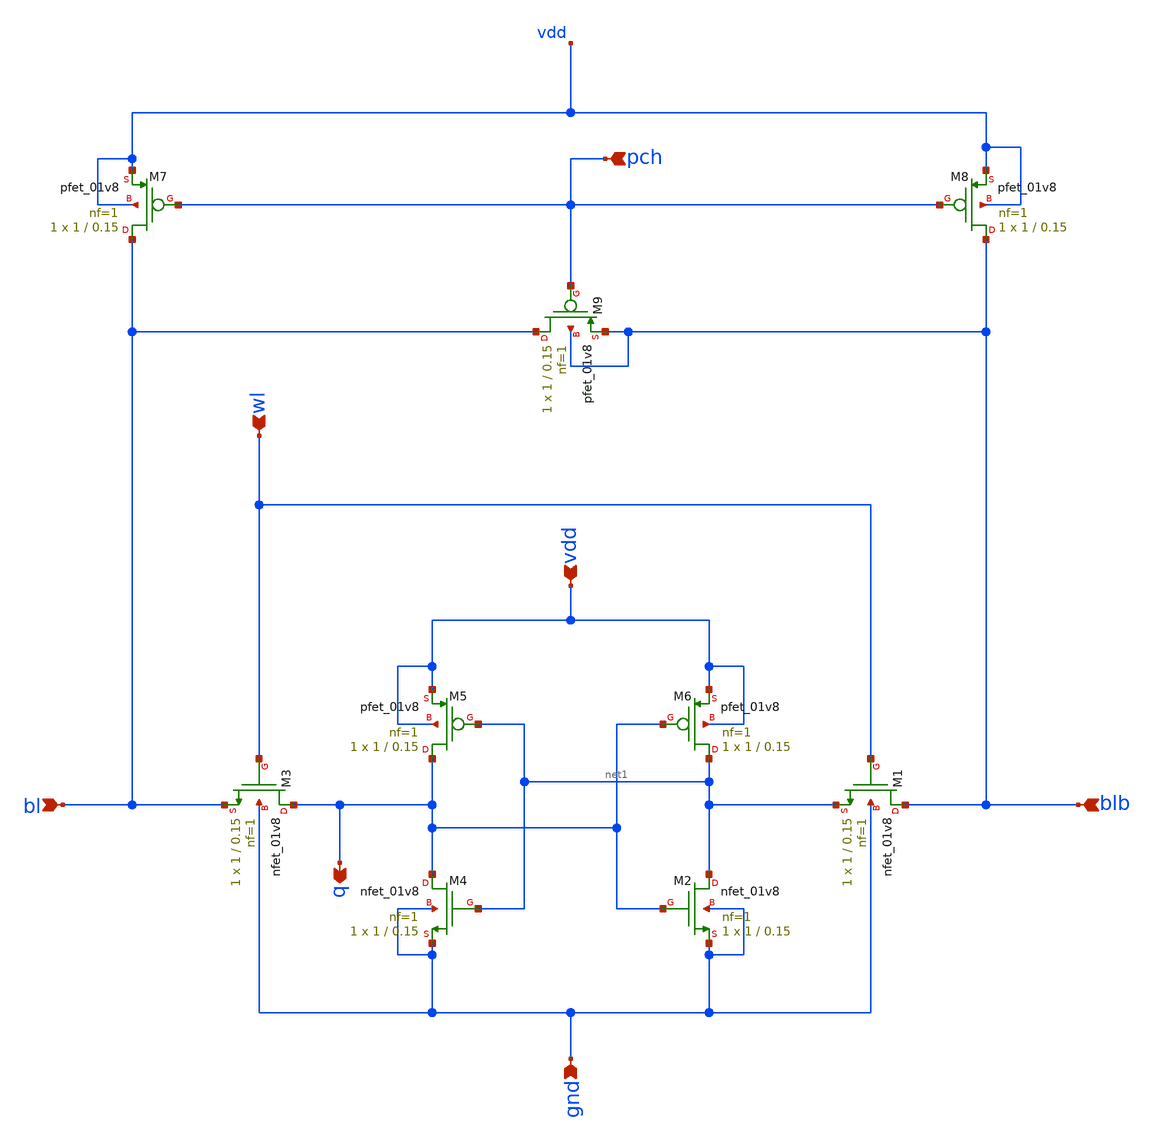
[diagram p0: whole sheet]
** sch_path: sram/sram_pch_1b.sch
**.subckt sram_pch_1b gnd bl blb vdd wl pch q
*.ipin gnd
*.ipin bl
*.ipin blb
*.ipin vdd
*.ipin wl
*.ipin pch
*.opin q
XM1 blb wl net1 gnd sky130_fd_pr__nfet_01v8 L=0.15 W=1 nf=1 ad='int((nf+1)/2) * W/nf * 0.29' as='int((nf+2)/2) * W/nf * 0.29'
+ pd='2*int((nf+1)/2) * (W/nf + 0.29)' ps='2*int((nf+2)/2) * (W/nf + 0.29)' nrd='0.29 / W' nrs='0.29 / W'
+ sa=0 sb=0 sd=0 mult=1 m=1
XM3 q wl bl gnd sky130_fd_pr__nfet_01v8 L=0.15 W=1 nf=1 ad='int((nf+1)/2) * W/nf * 0.29' as='int((nf+2)/2) * W/nf * 0.29'
+ pd='2*int((nf+1)/2) * (W/nf + 0.29)' ps='2*int((nf+2)/2) * (W/nf + 0.29)' nrd='0.29 / W' nrs='0.29 / W'
+ sa=0 sb=0 sd=0 mult=1 m=1
XM5 q net1 vdd vdd sky130_fd_pr__pfet_01v8 L=0.15 W=1 nf=1 ad='int((nf+1)/2) * W/nf * 0.29' as='int((nf+2)/2) * W/nf * 0.29'
+ pd='2*int((nf+1)/2) * (W/nf + 0.29)' ps='2*int((nf+2)/2) * (W/nf + 0.29)' nrd='0.29 / W' nrs='0.29 / W'
+ sa=0 sb=0 sd=0 mult=1 m=1
XM6 net1 q vdd vdd sky130_fd_pr__pfet_01v8 L=0.15 W=1 nf=1 ad='int((nf+1)/2) * W/nf * 0.29' as='int((nf+2)/2) * W/nf * 0.29'
+ pd='2*int((nf+1)/2) * (W/nf + 0.29)' ps='2*int((nf+2)/2) * (W/nf + 0.29)' nrd='0.29 / W' nrs='0.29 / W'
+ sa=0 sb=0 sd=0 mult=1 m=1
XM7 bl pch vdd vdd sky130_fd_pr__pfet_01v8 L=0.15 W=1 nf=1 ad='int((nf+1)/2) * W/nf * 0.29' as='int((nf+2)/2) * W/nf * 0.29'
+ pd='2*int((nf+1)/2) * (W/nf + 0.29)' ps='2*int((nf+2)/2) * (W/nf + 0.29)' nrd='0.29 / W' nrs='0.29 / W'
+ sa=0 sb=0 sd=0 mult=1 m=1
XM8 blb pch vdd vdd sky130_fd_pr__pfet_01v8 L=0.15 W=1 nf=1 ad='int((nf+1)/2) * W/nf * 0.29' as='int((nf+2)/2) * W/nf * 0.29'
+ pd='2*int((nf+1)/2) * (W/nf + 0.29)' ps='2*int((nf+2)/2) * (W/nf + 0.29)' nrd='0.29 / W' nrs='0.29 / W'
+ sa=0 sb=0 sd=0 mult=1 m=1
XM9 bl pch blb blb sky130_fd_pr__pfet_01v8 L=0.15 W=1 nf=1 ad='int((nf+1)/2) * W/nf * 0.29' as='int((nf+2)/2) * W/nf * 0.29'
+ pd='2*int((nf+1)/2) * (W/nf + 0.29)' ps='2*int((nf+2)/2) * (W/nf + 0.29)' nrd='0.29 / W' nrs='0.29 / W'
+ sa=0 sb=0 sd=0 mult=1 m=1
XM2 net1 q gnd gnd sky130_fd_pr__nfet_01v8 L=0.15 W=1 nf=1 ad='int((nf+1)/2) * W/nf * 0.29' as='int((nf+2)/2) * W/nf * 0.29'
+ pd='2*int((nf+1)/2) * (W/nf + 0.29)' ps='2*int((nf+2)/2) * (W/nf + 0.29)' nrd='0.29 / W' nrs='0.29 / W'
+ sa=0 sb=0 sd=0 mult=1 m=1
XM4 q net1 gnd gnd sky130_fd_pr__nfet_01v8 L=0.15 W=1 nf=1 ad='int((nf+1)/2) * W/nf * 0.29' as='int((nf+2)/2) * W/nf * 0.29'
+ pd='2*int((nf+1)/2) * (W/nf + 0.29)' ps='2*int((nf+2)/2) * (W/nf + 0.29)' nrd='0.29 / W' nrs='0.29 / W'
+ sa=0 sb=0 sd=0 mult=1 m=1
**.ends
.end
